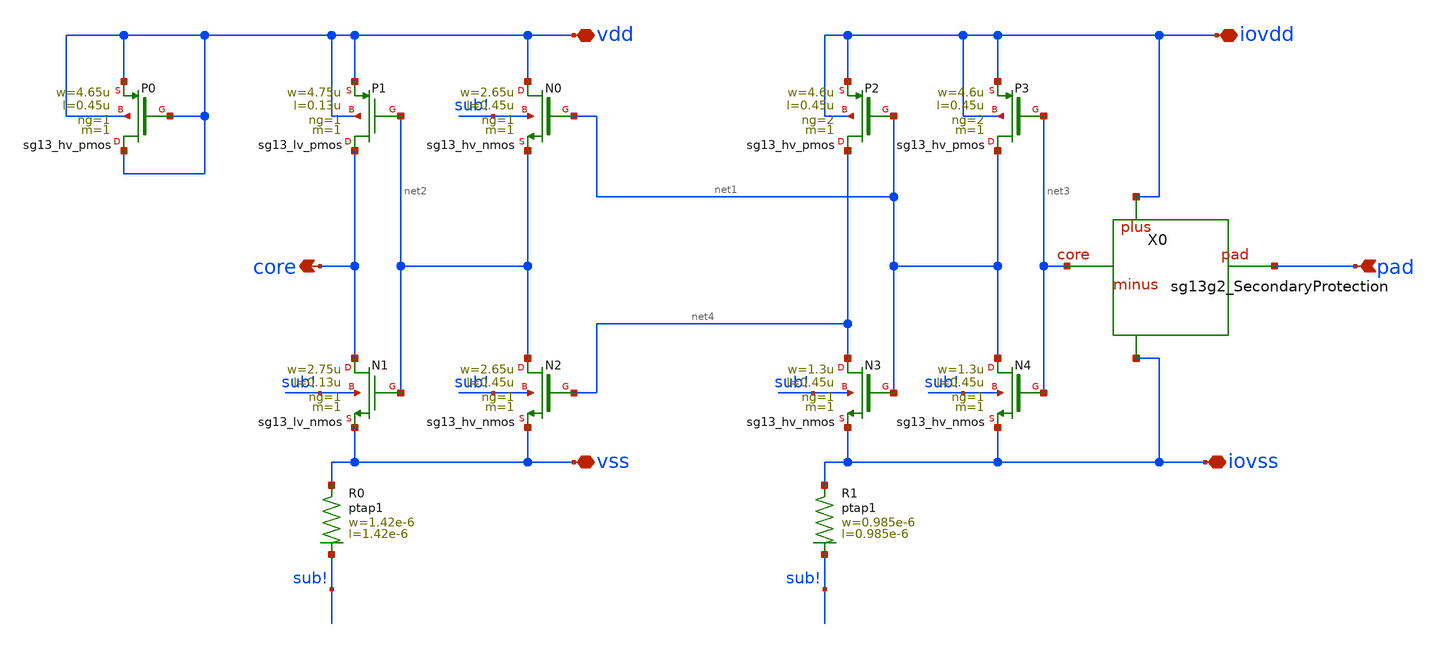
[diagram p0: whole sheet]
** sch_path: ihp-sg13g2/libs.ref/sg13g2_io/sch/xschem/sg13g2_LevelDown.sch
**.subckt sg13g2_LevelDown iovdd vdd core iovss vss pad
*.iopin iovdd
*.iopin vdd
*.opin core
*.iopin iovss
*.iopin vss
*.ipin pad
XN0 vdd net1 net2 sub! sg13_hv_nmos w=2.65u l=0.45u ng=1 m=1 mm_ok=1
XN1 core net2 vss sub! sg13_lv_nmos w=2.75u l=0.13u ng=1 m=1 mm_ok=1
XN2 net2 net4 vss sub! sg13_hv_nmos w=2.65u l=0.45u ng=1 m=1 mm_ok=1
XN3 net4 net1 iovss sub! sg13_hv_nmos w=1.3u l=0.45u ng=1 m=1 mm_ok=1
XN4 net1 net3 iovss sub! sg13_hv_nmos w=1.3u l=0.45u ng=1 m=1 mm_ok=1
XP0 vdd vdd vdd vdd sg13_hv_pmos w=4.65u l=0.45u ng=1 m=1 mm_ok=1
XP1 core net2 vdd vdd sg13_lv_pmos w=4.75u l=0.13u ng=1 m=1 mm_ok=1
XP2 net4 net1 iovdd iovdd sg13_hv_pmos w=4.6u l=0.45u ng=2 m=1 mm_ok=1
XP3 net1 net3 iovdd iovdd sg13_hv_pmos w=4.6u l=0.45u ng=2 m=1 mm_ok=1
X0 iovdd pad iovss net3 sg13g2_SecondaryProtection
XR0 vss sub! ptap1 R=127.3 w=1.42e-6 l=1.42e-6
XR1 iovss sub! ptap1 R=199.6 w=0.985e-6 l=0.985e-6
**.ends
.end
